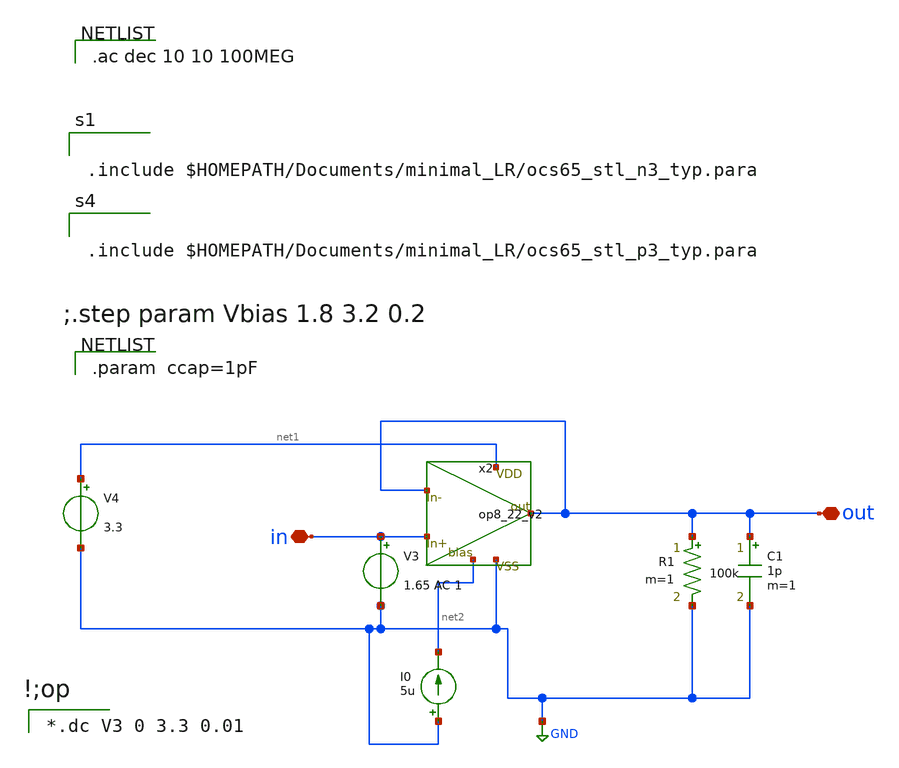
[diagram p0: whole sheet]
** sch_path: Xschem/op8_22_tb_direct.sch
**.subckt op8_22_tb_direct out in
*.iopin out
*.iopin in
x2 in out net1 GND net2 out op8_22_v2
V4 net1 GND 3.3
V3 in GND 1.65 AC 1
I0 GND net2 5u
R1 out GND 100k m=1
C1 out GND 1p m=1
**** begin user architecture code

.param  ccap=1pF


*.dc V3 0 3.3 0.01



.include $HOMEPATH/Documents/minimal_LR/ocs65_stl_p3_typ.para



.include $HOMEPATH/Documents/minimal_LR/ocs65_stl_n3_typ.para


.ac dec 10 10 100MEG

**** end user architecture code
**.ends
.GLOBAL GND
.end
